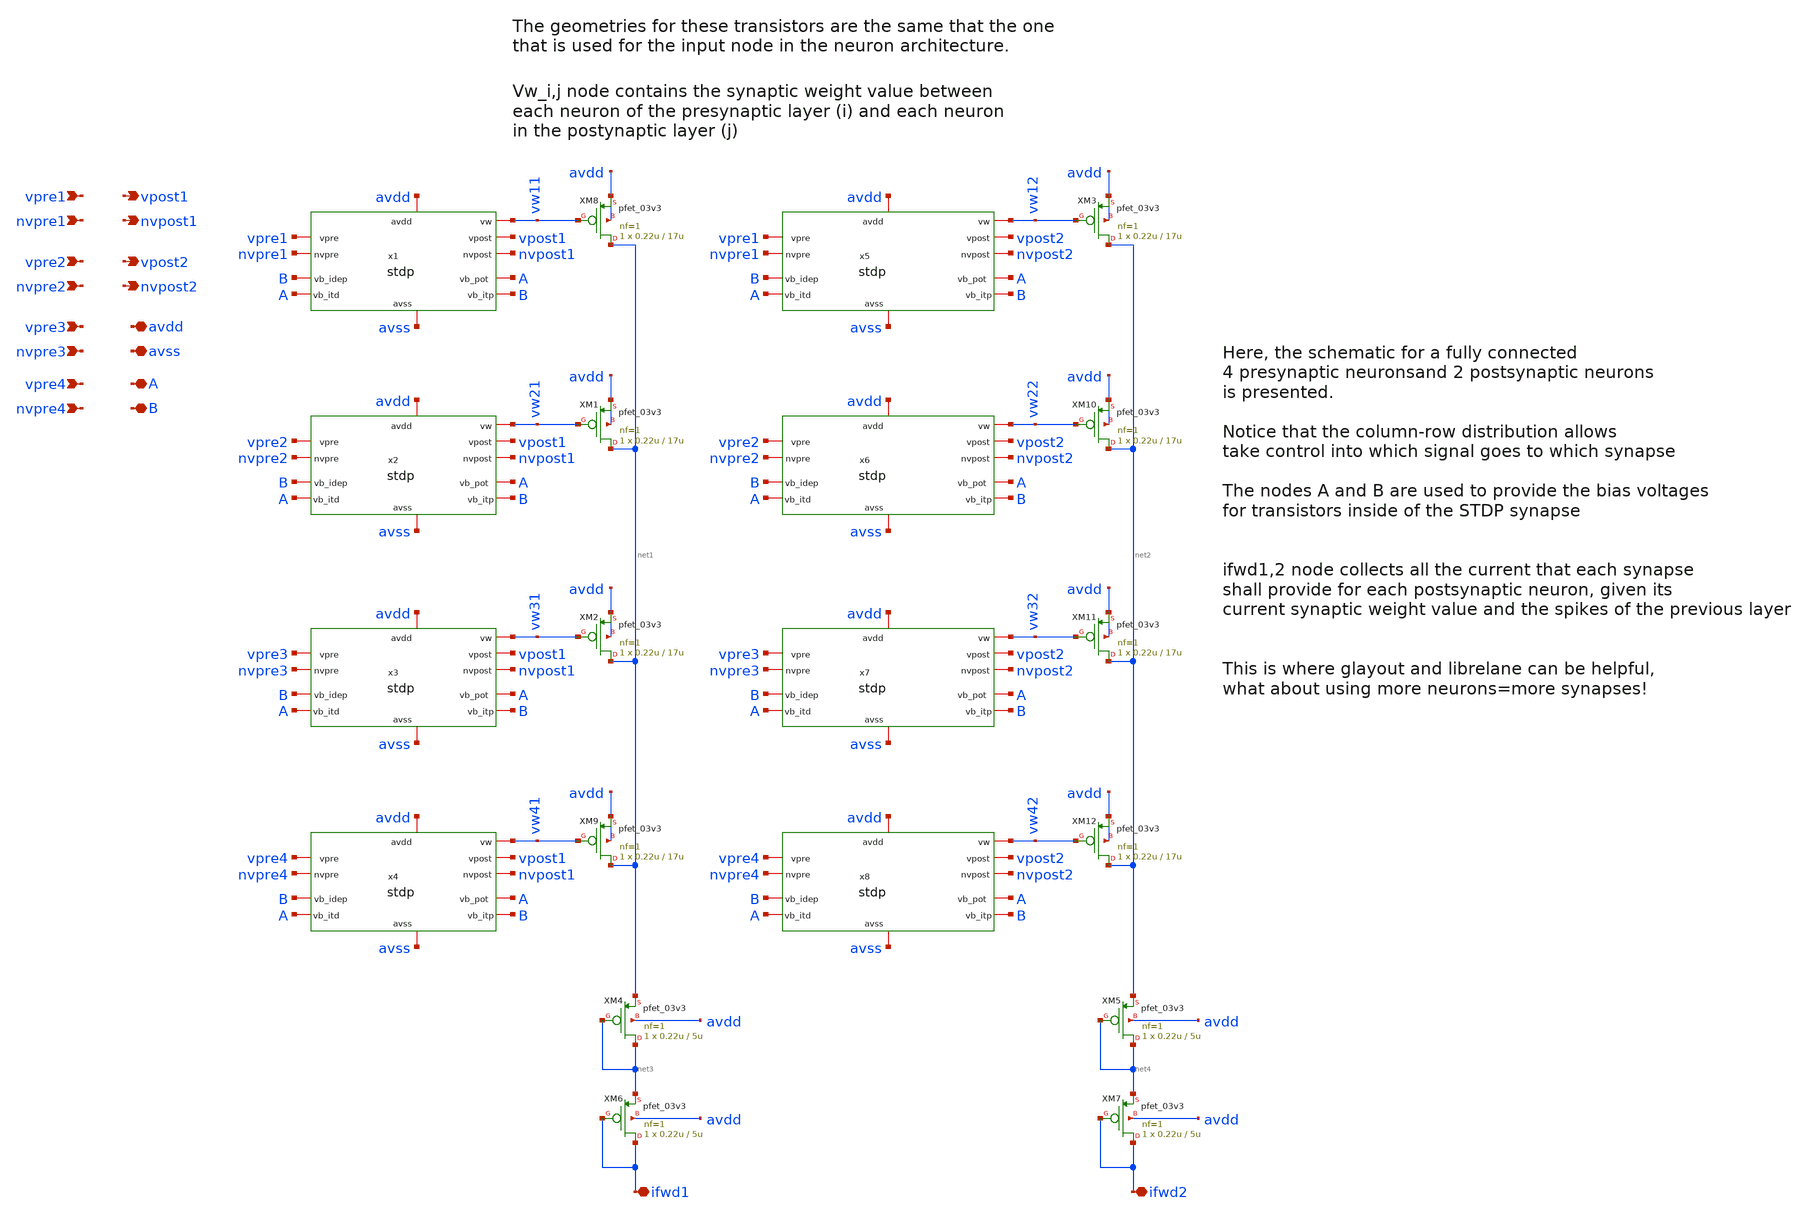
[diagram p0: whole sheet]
** sch_path: designs/libs/snn_analog/stdp/sch/stdp/stdp_4x2.sch
**.subckt stdp_4x2 ifwd1 ifwd2 vpre1 nvpre1 vpre2 nvpre2 vpre3 nvpre3 vpre4 nvpre4 vpost1 nvpost1
*+ vpost2 nvpost2 avdd avss A B
*.iopin ifwd1
*.iopin ifwd2
*.ipin vpre1
*.ipin nvpre1
*.ipin vpre2
*.ipin nvpre2
*.ipin vpre3
*.ipin nvpre3
*.ipin vpre4
*.ipin nvpre4
*.opin vpost1
*.opin nvpost1
*.opin vpost2
*.opin nvpost2
*.iopin avdd
*.iopin avss
*.iopin A
*.iopin B
x1 avdd avss nvpre1 nvpost1 vpre1 vpost1 A B B A vw11 stdp
x2 avdd avss nvpre2 nvpost1 vpre2 vpost1 A B B A vw21 stdp
x3 avdd avss nvpre3 nvpost1 vpre3 vpost1 A B B A vw31 stdp
x4 avdd avss nvpre4 nvpost1 vpre4 vpost1 A B B A vw41 stdp
x5 avdd avss nvpre1 nvpost2 vpre1 vpost2 A B B A vw12 stdp
x6 avdd avss nvpre2 nvpost2 vpre2 vpost2 A B B A vw22 stdp
x7 avdd avss nvpre3 nvpost2 vpre3 vpost2 A B B A vw32 stdp
x8 avdd avss nvpre4 nvpost2 vpre4 vpost2 A B B A vw42 stdp
XM8 net1 vw11 avdd avdd pfet_03v3 L=17u W=0.22u nf=1 ad='int((nf+1)/2) * W/nf * 0.18u' as='int((nf+2)/2) * W/nf * 0.18u'
+ pd='2*int((nf+1)/2) * (W/nf + 0.18u)' ps='2*int((nf+2)/2) * (W/nf + 0.18u)' nrd='0.18u / W' nrs='0.18u / W'
+ sa=0 sb=0 sd=0 m=1
XM1 net1 vw21 avdd avdd pfet_03v3 L=17u W=0.22u nf=1 ad='int((nf+1)/2) * W/nf * 0.18u' as='int((nf+2)/2) * W/nf * 0.18u'
+ pd='2*int((nf+1)/2) * (W/nf + 0.18u)' ps='2*int((nf+2)/2) * (W/nf + 0.18u)' nrd='0.18u / W' nrs='0.18u / W'
+ sa=0 sb=0 sd=0 m=1
XM2 net1 vw31 avdd avdd pfet_03v3 L=17u W=0.22u nf=1 ad='int((nf+1)/2) * W/nf * 0.18u' as='int((nf+2)/2) * W/nf * 0.18u'
+ pd='2*int((nf+1)/2) * (W/nf + 0.18u)' ps='2*int((nf+2)/2) * (W/nf + 0.18u)' nrd='0.18u / W' nrs='0.18u / W'
+ sa=0 sb=0 sd=0 m=1
XM9 net1 vw41 avdd avdd pfet_03v3 L=17u W=0.22u nf=1 ad='int((nf+1)/2) * W/nf * 0.18u' as='int((nf+2)/2) * W/nf * 0.18u'
+ pd='2*int((nf+1)/2) * (W/nf + 0.18u)' ps='2*int((nf+2)/2) * (W/nf + 0.18u)' nrd='0.18u / W' nrs='0.18u / W'
+ sa=0 sb=0 sd=0 m=1
XM3 net2 vw12 avdd avdd pfet_03v3 L=17u W=0.22u nf=1 ad='int((nf+1)/2) * W/nf * 0.18u' as='int((nf+2)/2) * W/nf * 0.18u'
+ pd='2*int((nf+1)/2) * (W/nf + 0.18u)' ps='2*int((nf+2)/2) * (W/nf + 0.18u)' nrd='0.18u / W' nrs='0.18u / W'
+ sa=0 sb=0 sd=0 m=1
XM10 net2 vw22 avdd avdd pfet_03v3 L=17u W=0.22u nf=1 ad='int((nf+1)/2) * W/nf * 0.18u' as='int((nf+2)/2) * W/nf * 0.18u'
+ pd='2*int((nf+1)/2) * (W/nf + 0.18u)' ps='2*int((nf+2)/2) * (W/nf + 0.18u)' nrd='0.18u / W' nrs='0.18u / W'
+ sa=0 sb=0 sd=0 m=1
XM11 net2 vw32 avdd avdd pfet_03v3 L=17u W=0.22u nf=1 ad='int((nf+1)/2) * W/nf * 0.18u' as='int((nf+2)/2) * W/nf * 0.18u'
+ pd='2*int((nf+1)/2) * (W/nf + 0.18u)' ps='2*int((nf+2)/2) * (W/nf + 0.18u)' nrd='0.18u / W' nrs='0.18u / W'
+ sa=0 sb=0 sd=0 m=1
XM12 net2 vw42 avdd avdd pfet_03v3 L=17u W=0.22u nf=1 ad='int((nf+1)/2) * W/nf * 0.18u' as='int((nf+2)/2) * W/nf * 0.18u'
+ pd='2*int((nf+1)/2) * (W/nf + 0.18u)' ps='2*int((nf+2)/2) * (W/nf + 0.18u)' nrd='0.18u / W' nrs='0.18u / W'
+ sa=0 sb=0 sd=0 m=1
XM4 net3 net3 net1 avdd pfet_03v3 L=5u W=0.22u nf=1 ad='int((nf+1)/2) * W/nf * 0.18u' as='int((nf+2)/2) * W/nf * 0.18u'
+ pd='2*int((nf+1)/2) * (W/nf + 0.18u)' ps='2*int((nf+2)/2) * (W/nf + 0.18u)' nrd='0.18u / W' nrs='0.18u / W'
+ sa=0 sb=0 sd=0 m=1
XM5 net4 net4 net2 avdd pfet_03v3 L=5u W=0.22u nf=1 ad='int((nf+1)/2) * W/nf * 0.18u' as='int((nf+2)/2) * W/nf * 0.18u'
+ pd='2*int((nf+1)/2) * (W/nf + 0.18u)' ps='2*int((nf+2)/2) * (W/nf + 0.18u)' nrd='0.18u / W' nrs='0.18u / W'
+ sa=0 sb=0 sd=0 m=1
XM6 ifwd1 ifwd1 net3 avdd pfet_03v3 L=5u W=0.22u nf=1 ad='int((nf+1)/2) * W/nf * 0.18u' as='int((nf+2)/2) * W/nf * 0.18u'
+ pd='2*int((nf+1)/2) * (W/nf + 0.18u)' ps='2*int((nf+2)/2) * (W/nf + 0.18u)' nrd='0.18u / W' nrs='0.18u / W'
+ sa=0 sb=0 sd=0 m=1
XM7 ifwd2 ifwd2 net4 avdd pfet_03v3 L=5u W=0.22u nf=1 ad='int((nf+1)/2) * W/nf * 0.18u' as='int((nf+2)/2) * W/nf * 0.18u'
+ pd='2*int((nf+1)/2) * (W/nf + 0.18u)' ps='2*int((nf+2)/2) * (W/nf + 0.18u)' nrd='0.18u / W' nrs='0.18u / W'
+ sa=0 sb=0 sd=0 m=1
**.ends
.end
